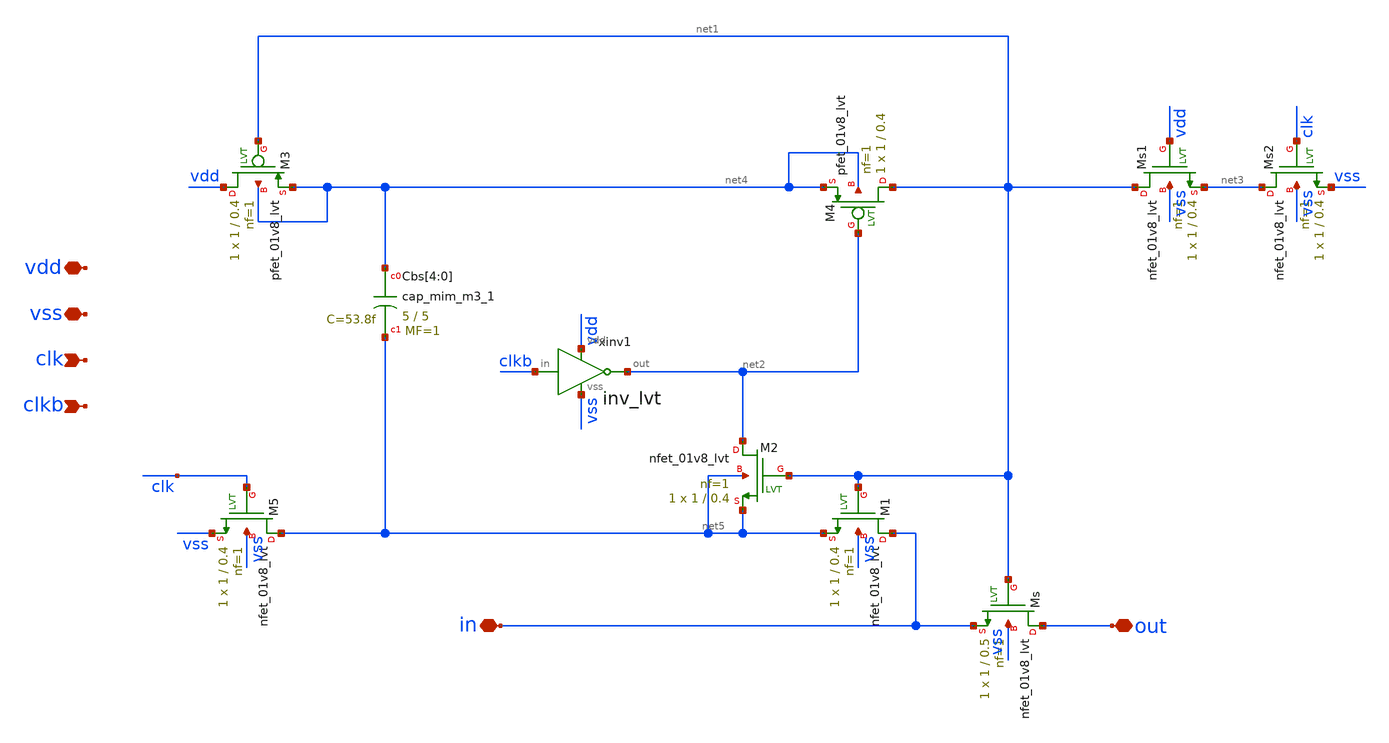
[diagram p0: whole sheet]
** sch_path: xschem/switches/bootstrapped_sw2.sch
**.subckt bootstrapped_sw2 out clk vss vdd in clkb
*.iopin out
*.ipin clk
*.iopin vss
*.iopin vdd
*.iopin in
*.ipin clkb
xinv1 vdd clkb net2 vss inv_lvt
XMs out net1 in vss sky130_fd_pr__nfet_01v8_lvt L=0.5 W=1 nf=1 ad='int((nf+1)/2) * W/nf * 0.29' as='int((nf+2)/2) * W/nf * 0.29'
+ pd='2*int((nf+1)/2) * (W/nf + 0.29)' ps='2*int((nf+2)/2) * (W/nf + 0.29)' nrd='0.29 / W' nrs='0.29 / W'
+ sa=0 sb=0 sd=0 mult=1 m=1
XMs1 net1 vdd net3 vss sky130_fd_pr__nfet_01v8_lvt L=0.4 W=1 nf=1 ad='int((nf+1)/2) * W/nf * 0.29' as='int((nf+2)/2) * W/nf * 0.29'
+ pd='2*int((nf+1)/2) * (W/nf + 0.29)' ps='2*int((nf+2)/2) * (W/nf + 0.29)' nrd='0.29 / W' nrs='0.29 / W'
+ sa=0 sb=0 sd=0 mult=1 m=1
XMs2 net3 clk vss vss sky130_fd_pr__nfet_01v8_lvt L=0.4 W=1 nf=1 ad='int((nf+1)/2) * W/nf * 0.29' as='int((nf+2)/2) * W/nf * 0.29'
+ pd='2*int((nf+1)/2) * (W/nf + 0.29)' ps='2*int((nf+2)/2) * (W/nf + 0.29)' nrd='0.29 / W' nrs='0.29 / W'
+ sa=0 sb=0 sd=0 mult=1 m=1
XM4 net1 net2 net4 net4 sky130_fd_pr__pfet_01v8_lvt L=0.4 W=1 nf=1 ad='int((nf+1)/2) * W/nf * 0.29' as='int((nf+2)/2) * W/nf * 0.29'
+ pd='2*int((nf+1)/2) * (W/nf + 0.29)' ps='2*int((nf+2)/2) * (W/nf + 0.29)' nrd='0.29 / W' nrs='0.29 / W'
+ sa=0 sb=0 sd=0 mult=1 m=1
XM1 in net1 net5 vss sky130_fd_pr__nfet_01v8_lvt L=0.4 W=1 nf=1 ad='int((nf+1)/2) * W/nf * 0.29' as='int((nf+2)/2) * W/nf * 0.29'
+ pd='2*int((nf+1)/2) * (W/nf + 0.29)' ps='2*int((nf+2)/2) * (W/nf + 0.29)' nrd='0.29 / W' nrs='0.29 / W'
+ sa=0 sb=0 sd=0 mult=1 m=1
XM2 net2 net1 net5 net5 sky130_fd_pr__nfet_01v8_lvt L=0.4 W=1 nf=1 ad='int((nf+1)/2) * W/nf * 0.29' as='int((nf+2)/2) * W/nf * 0.29'
+ pd='2*int((nf+1)/2) * (W/nf + 0.29)' ps='2*int((nf+2)/2) * (W/nf + 0.29)' nrd='0.29 / W' nrs='0.29 / W'
+ sa=0 sb=0 sd=0 mult=1 m=1
XM3 vdd net1 net4 net4 sky130_fd_pr__pfet_01v8_lvt L=0.4 W=1 nf=1 ad='int((nf+1)/2) * W/nf * 0.29' as='int((nf+2)/2) * W/nf * 0.29'
+ pd='2*int((nf+1)/2) * (W/nf + 0.29)' ps='2*int((nf+2)/2) * (W/nf + 0.29)' nrd='0.29 / W' nrs='0.29 / W'
+ sa=0 sb=0 sd=0 mult=1 m=1
XCbs[4] net4 net5 sky130_fd_pr__cap_mim_m3_1 W=5 L=5 MF=1 m=1
XCbs[3] net4 net5 sky130_fd_pr__cap_mim_m3_1 W=5 L=5 MF=1 m=1
XCbs[2] net4 net5 sky130_fd_pr__cap_mim_m3_1 W=5 L=5 MF=1 m=1
XCbs[1] net4 net5 sky130_fd_pr__cap_mim_m3_1 W=5 L=5 MF=1 m=1
XCbs[0] net4 net5 sky130_fd_pr__cap_mim_m3_1 W=5 L=5 MF=1 m=1
XM5 net5 clk vss vss sky130_fd_pr__nfet_01v8_lvt L=0.4 W=1 nf=1 ad='int((nf+1)/2) * W/nf * 0.29' as='int((nf+2)/2) * W/nf * 0.29'
+ pd='2*int((nf+1)/2) * (W/nf + 0.29)' ps='2*int((nf+2)/2) * (W/nf + 0.29)' nrd='0.29 / W' nrs='0.29 / W'
+ sa=0 sb=0 sd=0 mult=1 m=1
**.ends

* expanding   symbol:  logic/inv_lvt.sym # of pins=4
** sym_path: logic/inv_lvt.sym
** sch_path: logic/inv_lvt.sch
.subckt inv_lvt vdd in out vss
*.iopin vdd
*.iopin vss
*.ipin in
*.opin out
XM1 out in vss vss sky130_fd_pr__nfet_01v8_lvt L=0.4 W=1 nf=1 ad='int((nf+1)/2) * W/nf * 0.29' as='int((nf+2)/2) * W/nf * 0.29'
+ pd='2*int((nf+1)/2) * (W/nf + 0.29)' ps='2*int((nf+2)/2) * (W/nf + 0.29)' nrd='0.29 / W' nrs='0.29 / W'
+ sa=0 sb=0 sd=0 mult=1 m=1
XM2 out in vdd vdd sky130_fd_pr__pfet_01v8_lvt L=0.4 W=1 nf=1 ad='int((nf+1)/2) * W/nf * 0.29' as='int((nf+2)/2) * W/nf * 0.29'
+ pd='2*int((nf+1)/2) * (W/nf + 0.29)' ps='2*int((nf+2)/2) * (W/nf + 0.29)' nrd='0.29 / W' nrs='0.29 / W'
+ sa=0 sb=0 sd=0 mult=1 m=1
.ends

.end
